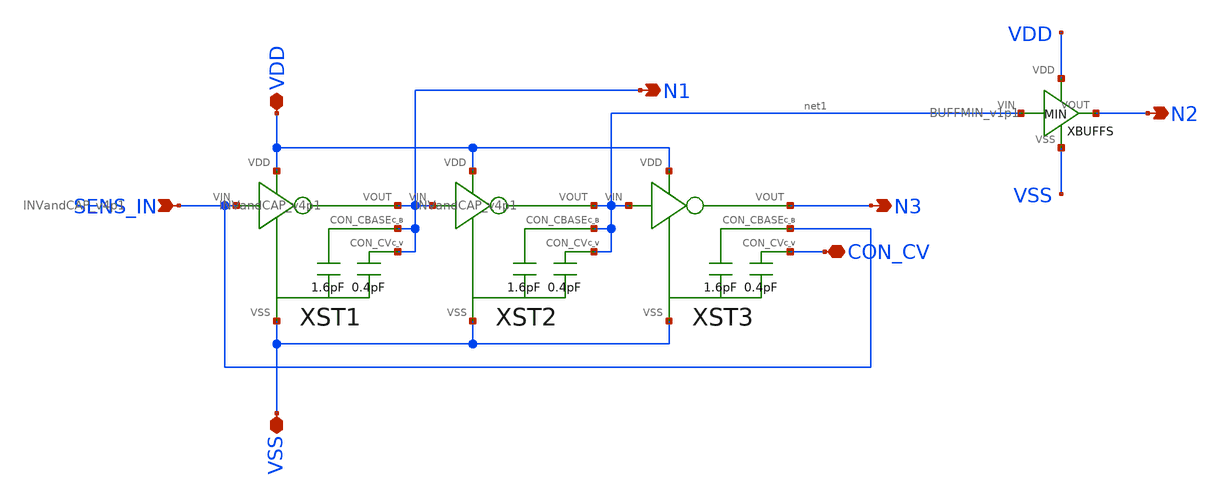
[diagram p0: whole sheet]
** sch_path: modules/OSC_v7p1/symbol/OSC_v7p1.sch
**.subckt OSC_v7p1 SENS_IN VDD VSS N1 N2 CON_CV N3
*.ipin SENS_IN
*.iopin VDD
*.iopin VSS
*.opin N1
*.opin N2
*.iopin CON_CV
*.opin N3
XST1 SENS_IN VDD VSS N1 N1 N1 INVandCAP_v4p1
XST2 N1 VDD VSS net1 net1 net1 INVandCAP_v4p1
XST3 net1 VDD VSS N3 CON_CV SENS_IN INVandCAP_v4p1
XBUFFS net1 N2 VDD VSS BUFFMIN_v1p1
**.ends
.end
